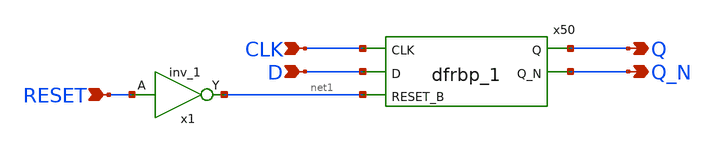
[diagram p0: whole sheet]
** sch_path: xschem/untitled.sch
**.subckt untitled CLK D RESET Q Q_N
*.ipin CLK
*.ipin D
*.ipin RESET
*.opin Q
*.opin Q_N
x50 CLK D net1 dvss dvss dvdd dvdd Q Q_N sky130_fd_sc_hd__dfrbp_1
x1 RESET GND GND VDD VDD net1 sky130_fd_sc_hd__inv_1
**.ends
.end
